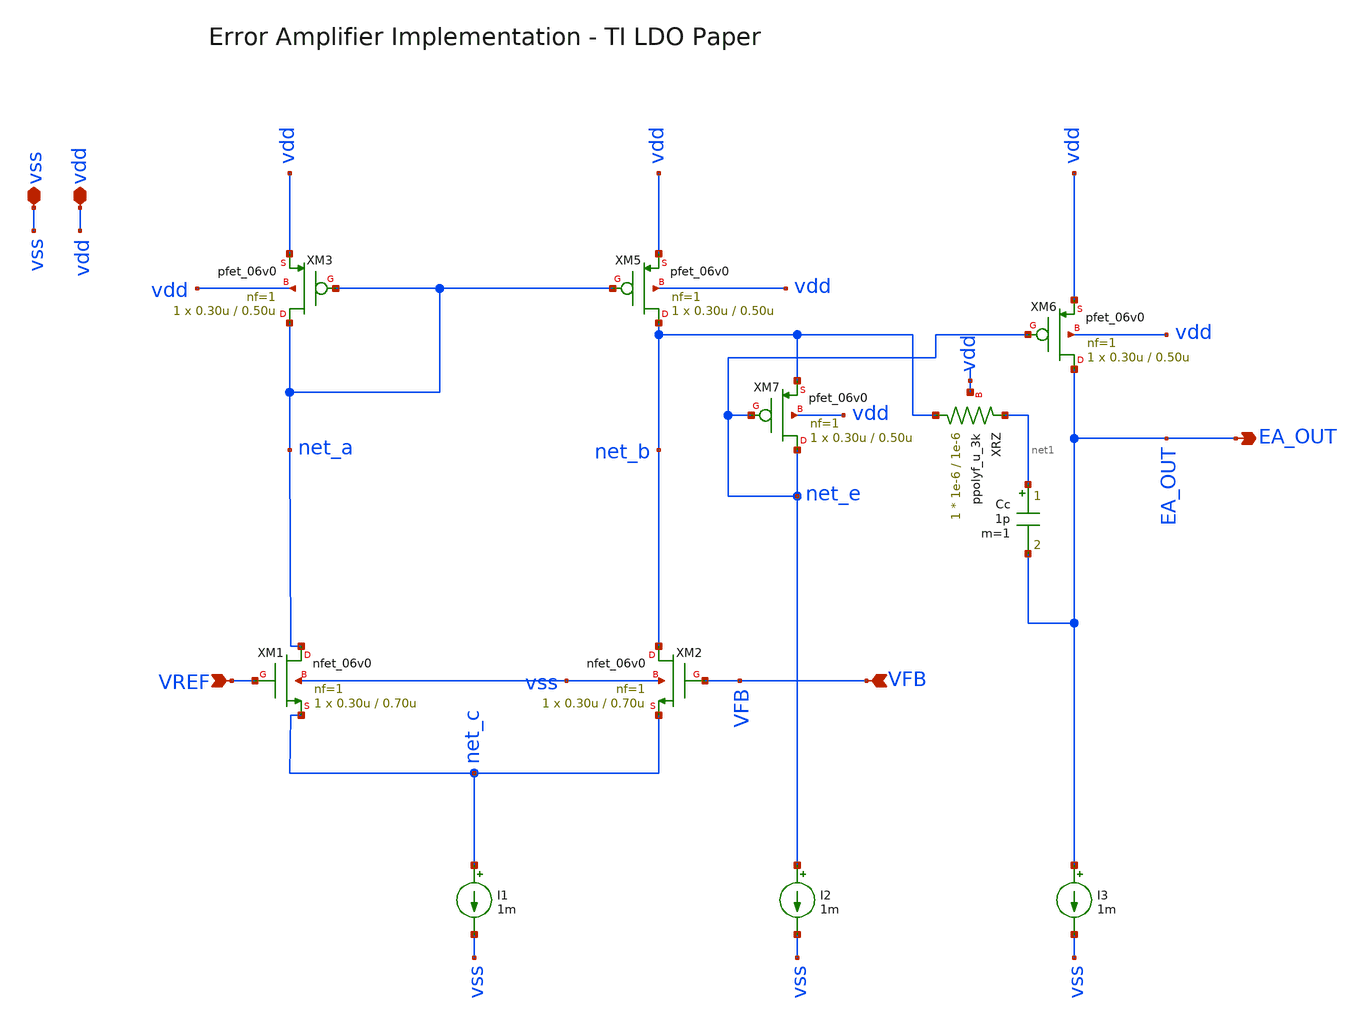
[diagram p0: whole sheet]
** sch_path: analog-db/circuits/ldo_005_buffered_ref/reference/ti-ldo/error_amp/error_amp_diode_connected.sch
**.subckt error_amp_diode_connected vdd vss VFB EA_OUT VREF
*.iopin vdd
*.iopin vss
*.ipin VFB
*.opin EA_OUT
*.ipin VREF
XM2 net_b VFB net_c vss nfet_06v0 L=0.70u W=0.30u nf=1 ad='int((nf+1)/2) * W/nf * 0.18u' as='int((nf+2)/2) * W/nf * 0.18u'
+ pd='2*int((nf+1)/2) * (W/nf + 0.18u)' ps='2*int((nf+2)/2) * (W/nf + 0.18u)' nrd='0.18u / W' nrs='0.18u / W'
+ sa=0 sb=0 sd=0 m=1
I1 net_c vss 1m
I2 net_e vss 1m
I3 EA_OUT vss 1m
XM3 net_a net_a vdd vdd pfet_06v0 L=0.50u W=0.30u nf=1 ad='int((nf+1)/2) * W/nf * 0.18u' as='int((nf+2)/2) * W/nf * 0.18u'
+ pd='2*int((nf+1)/2) * (W/nf + 0.18u)' ps='2*int((nf+2)/2) * (W/nf + 0.18u)' nrd='0.18u / W' nrs='0.18u / W'
+ sa=0 sb=0 sd=0 m=1
XM5 net_b net_a vdd vdd pfet_06v0 L=0.50u W=0.30u nf=1 ad='int((nf+1)/2) * W/nf * 0.18u' as='int((nf+2)/2) * W/nf * 0.18u'
+ pd='2*int((nf+1)/2) * (W/nf + 0.18u)' ps='2*int((nf+2)/2) * (W/nf + 0.18u)' nrd='0.18u / W' nrs='0.18u / W'
+ sa=0 sb=0 sd=0 m=1
XM6 EA_OUT net_e vdd vdd pfet_06v0 L=0.50u W=0.30u nf=1 ad='int((nf+1)/2) * W/nf * 0.18u' as='int((nf+2)/2) * W/nf * 0.18u'
+ pd='2*int((nf+1)/2) * (W/nf + 0.18u)' ps='2*int((nf+2)/2) * (W/nf + 0.18u)' nrd='0.18u / W' nrs='0.18u / W'
+ sa=0 sb=0 sd=0 m=1
XM7 net_e net_e net_b vdd pfet_06v0 L=0.50u W=0.30u nf=1 ad='int((nf+1)/2) * W/nf * 0.18u' as='int((nf+2)/2) * W/nf * 0.18u'
+ pd='2*int((nf+1)/2) * (W/nf + 0.18u)' ps='2*int((nf+2)/2) * (W/nf + 0.18u)' nrd='0.18u / W' nrs='0.18u / W'
+ sa=0 sb=0 sd=0 m=1
Cc net1 EA_OUT 1p m=1
XRZ net_b net1 vdd ppolyf_u_3k r_width=1e-6 r_length=1e-6 m=1
XM1 net_a VREF net_c vss nfet_06v0 L=0.70u W=0.30u nf=1 ad='int((nf+1)/2) * W/nf * 0.18u' as='int((nf+2)/2) * W/nf * 0.18u'
+ pd='2*int((nf+1)/2) * (W/nf + 0.18u)' ps='2*int((nf+2)/2) * (W/nf + 0.18u)' nrd='0.18u / W' nrs='0.18u / W'
+ sa=0 sb=0 sd=0 m=1
**.ends
.end
